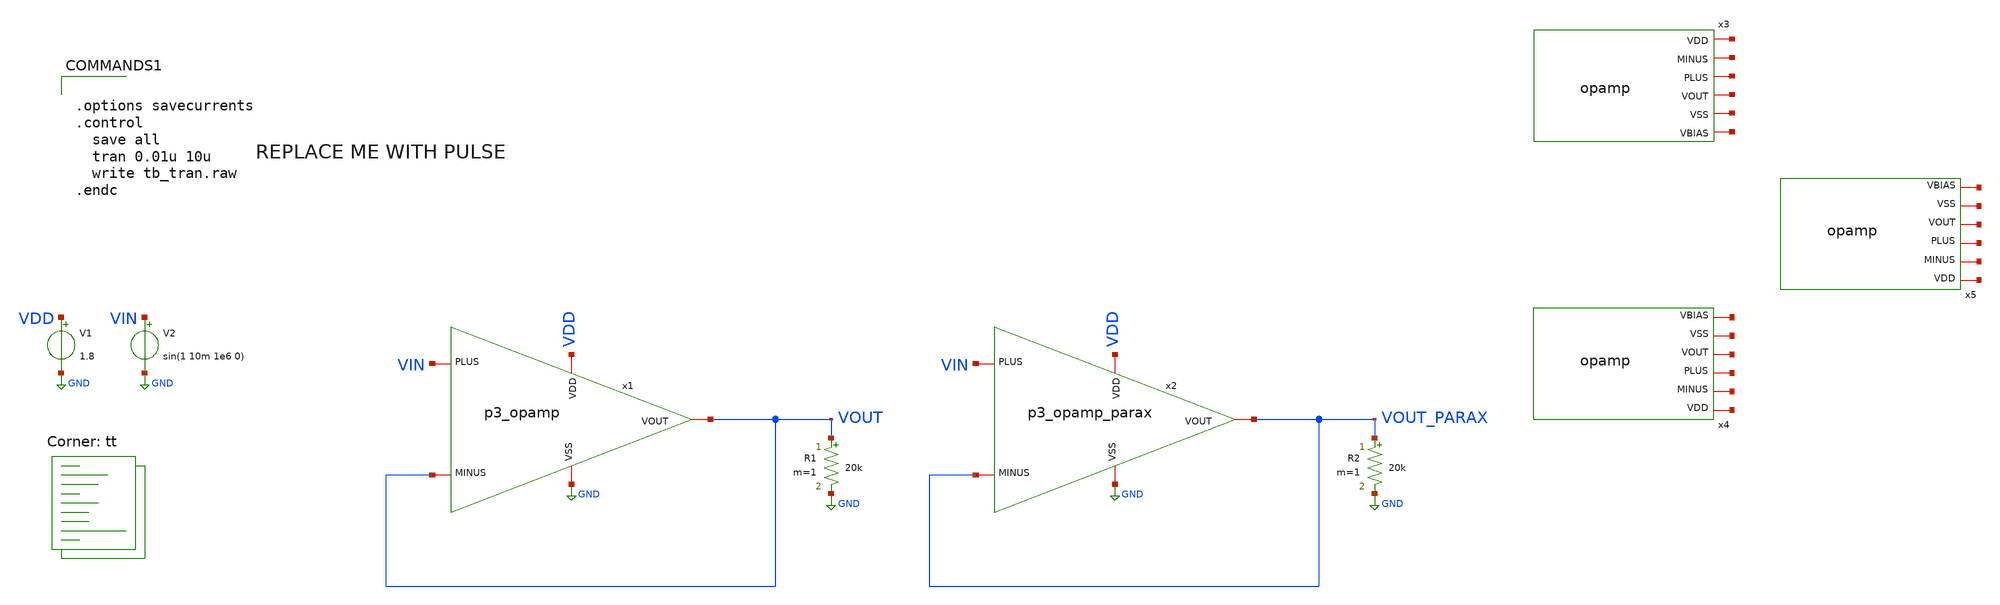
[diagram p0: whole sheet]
** sch_path: xschem/tb_opamp_tran.sch
**.subckt tb_opamp_tran
V1 VDD GND 1.8
V2 VIN GND sin(1 10m 1e6 0)
R1 VOUT GND 20k m=1
x1 VDD VOUT VIN VOUT GND p3_opamp
R2 VOUT_PARAX GND 20k m=1
x2 VDD VOUT_PARAX VIN VOUT_PARAX GND p3_opamp_parax
x3 net1 net2 net3 net4 net5 net6 opamp
x4 net7 net8 net9 net10 net11 net12 opamp
x5 net13 net14 net15 net16 net17 net18 opamp
**** begin user architecture code
.lib $::SKYWATER_MODELS/sky130.lib.spice tt


.options savecurrents
.control
  save all
  tran 0.01u 10u
  write tb_tran.raw
.endc


**** end user architecture code
**.ends
.GLOBAL GND
.end
